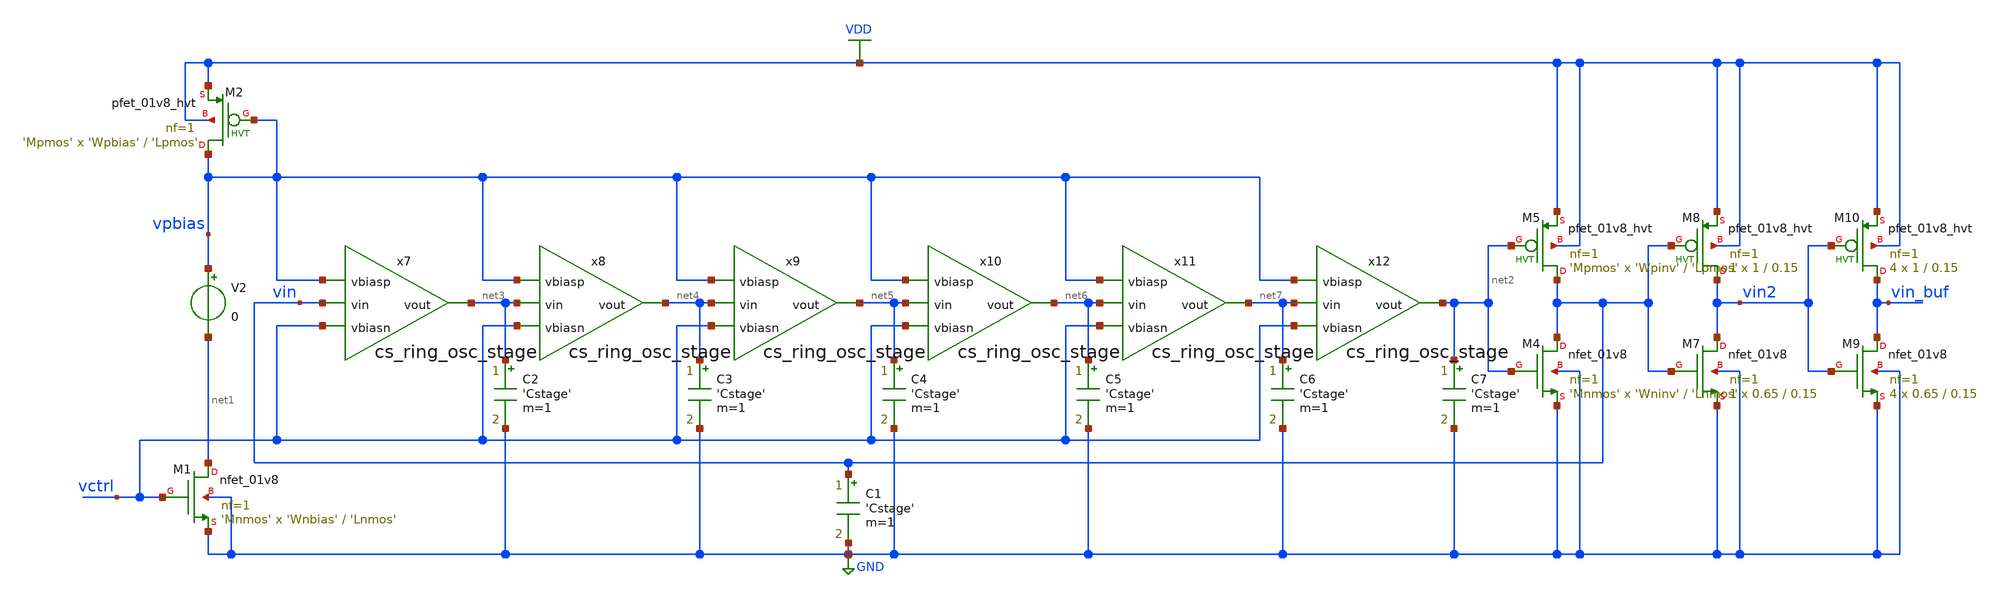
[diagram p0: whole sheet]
** sch_path: designs/cs_ring_osc_tb.sch
* Copyright 2020 Stefan Frederik Schippers
* Licensed under the Apache License, Version 2.0 (the "License");
* you may not use this file except in compliance with the License.
* You may obtain a copy of the License at
* https://www.apache.org/licenses/LICENSE-2.0
* Unless required by applicable law or agreed to in writing, software
* distributed under the License is distributed on an "AS IS" BASIS,
* WITHOUT WARRANTIES OR CONDITIONS OF ANY KIND, either express or implied.
* See the License for the specific language governing permissions and
* limitations under the License.
**.subckt cs_ring_osc_tb
V2 vpbias net1 0
XM1 net1 vctrl GND GND sky130_fd_pr__nfet_01v8 L='Lnmos' W='Wnbias' nf=1 ad='int((nf+1)/2) * W/nf * 0.29'
+ as='int((nf+2)/2) * W/nf * 0.29' pd='2*int((nf+1)/2) * (W/nf + 0.29)' ps='2*int((nf+2)/2) * (W/nf + 0.29)'
+ nrd='0.29 / W' nrs='0.29 / W' sa=0 sb=0 sd=0 mult='Mnmos' m='Mnmos'
XM2 vpbias vpbias VDD VDD sky130_fd_pr__pfet_01v8_hvt L='Lpmos' W='Wpbias' nf=1 ad='int((nf+1)/2) * W/nf * 0.29'
+ as='int((nf+2)/2) * W/nf * 0.29' pd='2*int((nf+1)/2) * (W/nf + 0.29)' ps='2*int((nf+2)/2) * (W/nf + 0.29)'
+ nrd='0.29 / W' nrs='0.29 / W' sa=0 sb=0 sd=0 mult='Mpmos' m='Mpmos'
x7 vpbias net3 vin vctrl cs_ring_osc_stage
x8 vpbias net4 net3 vctrl cs_ring_osc_stage
x9 vpbias net5 net4 vctrl cs_ring_osc_stage
x10 vpbias net6 net5 vctrl cs_ring_osc_stage
x11 vpbias net7 net6 vctrl cs_ring_osc_stage
x12 vpbias net2 net7 vctrl cs_ring_osc_stage
XM4 vin net2 GND GND sky130_fd_pr__nfet_01v8 L='Lnmos' W='Wninv' nf=1 ad='int((nf+1)/2) * W/nf * 0.29'
+ as='int((nf+2)/2) * W/nf * 0.29' pd='2*int((nf+1)/2) * (W/nf + 0.29)' ps='2*int((nf+2)/2) * (W/nf + 0.29)'
+ nrd='0.29 / W' nrs='0.29 / W' sa=0 sb=0 sd=0 mult='Mnmos' m='Mnmos'
XM5 vin net2 VDD VDD sky130_fd_pr__pfet_01v8_hvt L='Lpmos' W='Wpinv' nf=1 ad='int((nf+1)/2) * W/nf * 0.29'
+ as='int((nf+2)/2) * W/nf * 0.29' pd='2*int((nf+1)/2) * (W/nf + 0.29)' ps='2*int((nf+2)/2) * (W/nf + 0.29)'
+ nrd='0.29 / W' nrs='0.29 / W' sa=0 sb=0 sd=0 mult='Mpmos' m='Mpmos'
C1 vin GND 'Cstage' m=1
XM7 vin2 vin GND GND sky130_fd_pr__nfet_01v8 L=0.15 W=0.65 nf=1 ad='int((nf+1)/2) * W/nf * 0.29' as='int((nf+2)/2) * W/nf * 0.29'
+ pd='2*int((nf+1)/2) * (W/nf + 0.29)' ps='2*int((nf+2)/2) * (W/nf + 0.29)' nrd='0.29 / W' nrs='0.29 / W'
+ sa=0 sb=0 sd=0 mult=1 m=1
XM8 vin2 vin VDD VDD sky130_fd_pr__pfet_01v8_hvt L=0.15 W=1 nf=1 ad='int((nf+1)/2) * W/nf * 0.29' as='int((nf+2)/2) * W/nf * 0.29'
+ pd='2*int((nf+1)/2) * (W/nf + 0.29)' ps='2*int((nf+2)/2) * (W/nf + 0.29)' nrd='0.29 / W' nrs='0.29 / W'
+ sa=0 sb=0 sd=0 mult=1 m=1
XM9 vin_buf vin2 GND GND sky130_fd_pr__nfet_01v8 L=0.15 W=0.65 nf=1 ad='int((nf+1)/2) * W/nf * 0.29'
+ as='int((nf+2)/2) * W/nf * 0.29' pd='2*int((nf+1)/2) * (W/nf + 0.29)' ps='2*int((nf+2)/2) * (W/nf + 0.29)'
+ nrd='0.29 / W' nrs='0.29 / W' sa=0 sb=0 sd=0 mult=4 m=4
XM10 vin_buf vin2 VDD VDD sky130_fd_pr__pfet_01v8_hvt L=0.15 W=1 nf=1 ad='int((nf+1)/2) * W/nf * 0.29'
+ as='int((nf+2)/2) * W/nf * 0.29' pd='2*int((nf+1)/2) * (W/nf + 0.29)' ps='2*int((nf+2)/2) * (W/nf + 0.29)'
+ nrd='0.29 / W' nrs='0.29 / W' sa=0 sb=0 sd=0 mult=4 m=4
C2 net3 GND 'Cstage' m=1
C3 net4 GND 'Cstage' m=1
C4 net5 GND 'Cstage' m=1
C5 net6 GND 'Cstage' m=1
C6 net7 GND 'Cstage' m=1
C7 net2 GND 'Cstage' m=1
**** begin user architecture code

.include $::SKYWATER_MODELS/cells/nfet_01v8/sky130_fd_pr__nfet_01v8__tt.corner.spice
.include $::SKYWATER_MODELS/cells/nfet_01v8_lvt/sky130_fd_pr__nfet_01v8_lvt__tt.corner.spice
.include $::SKYWATER_MODELS/cells/pfet_01v8/sky130_fd_pr__pfet_01v8__tt.corner.spice
.include $::SKYWATER_MODELS/cells/nfet_03v3_nvt/sky130_fd_pr__nfet_03v3_nvt__tt.corner.spice
.include $::SKYWATER_MODELS/cells/nfet_05v0_nvt/sky130_fd_pr__nfet_05v0_nvt__tt.corner.spice
.include $::SKYWATER_MODELS/cells/esd_nfet_01v8/sky130_fd_pr__esd_nfet_01v8__tt.corner.spice
.include $::SKYWATER_MODELS/cells/pfet_01v8_lvt/sky130_fd_pr__pfet_01v8_lvt__tt.corner.spice
.include $::SKYWATER_MODELS/cells/pfet_01v8_hvt/sky130_fd_pr__pfet_01v8_hvt__tt.corner.spice
.include $::SKYWATER_MODELS/cells/esd_pfet_g5v0d10v5/sky130_fd_pr__esd_pfet_g5v0d10v5__tt.corner.spice
.include $::SKYWATER_MODELS/cells/pfet_g5v0d10v5/sky130_fd_pr__pfet_g5v0d10v5__tt.corner.spice
.include $::SKYWATER_MODELS/cells/pfet_g5v0d16v0/sky130_fd_pr__pfet_g5v0d16v0__tt.corner.spice
.include $::SKYWATER_MODELS/cells/nfet_g5v0d10v5/sky130_fd_pr__nfet_g5v0d10v5__tt.corner.spice
.include $::SKYWATER_MODELS/cells/nfet_g5v0d16v0/sky130_fd_pr__nfet_g5v0d16v0__tt_discrete.corner.spice
.include $::SKYWATER_MODELS/cells/esd_nfet_g5v0d10v5/sky130_fd_pr__esd_nfet_g5v0d10v5__tt.corner.spice
.include $::SKYWATER_MODELS/models/corners/tt/nonfet.spice
* Mismatch parameters
.include $::SKYWATER_MODELS/cells/nfet_01v8/sky130_fd_pr__nfet_01v8__mismatch.corner.spice
.include $::SKYWATER_MODELS/cells/pfet_01v8/sky130_fd_pr__pfet_01v8__mismatch.corner.spice
.include $::SKYWATER_MODELS/cells/nfet_01v8_lvt/sky130_fd_pr__nfet_01v8_lvt__mismatch.corner.spice
.include $::SKYWATER_MODELS/cells/pfet_01v8_lvt/sky130_fd_pr__pfet_01v8_lvt__mismatch.corner.spice
.include $::SKYWATER_MODELS/cells/pfet_01v8_hvt/sky130_fd_pr__pfet_01v8_hvt__mismatch.corner.spice
.include $::SKYWATER_MODELS/cells/nfet_g5v0d10v5/sky130_fd_pr__nfet_g5v0d10v5__mismatch.corner.spice
.include $::SKYWATER_MODELS/cells/pfet_g5v0d10v5/sky130_fd_pr__pfet_g5v0d10v5__mismatch.corner.spice
.include $::SKYWATER_MODELS/cells/nfet_05v0_nvt/sky130_fd_pr__nfet_05v0_nvt__mismatch.corner.spice
.include $::SKYWATER_MODELS/cells/nfet_03v3_nvt/sky130_fd_pr__nfet_03v3_nvt__mismatch.corner.spice
* Resistor$::SKYWATER_MODELS/Capacitor
.include $::SKYWATER_MODELS/models/r+c/res_typical__cap_typical.spice
.include $::SKYWATER_MODELS/models/r+c/res_typical__cap_typical__lin.spice
* Special cells
.include $::SKYWATER_MODELS/models/corners/tt/specialized_cells.spice
* All models
.include $::SKYWATER_MODELS/models/all.spice
* Corner
.include $::SKYWATER_MODELS/models/corners/tt/rf.spice

**** end user architecture code
**.ends
.GLOBAL VDD
.GLOBAL GND
**** begin user architecture code

.include cs_ring_osc_tb_commands.spice

**** end user architecture code
.end
